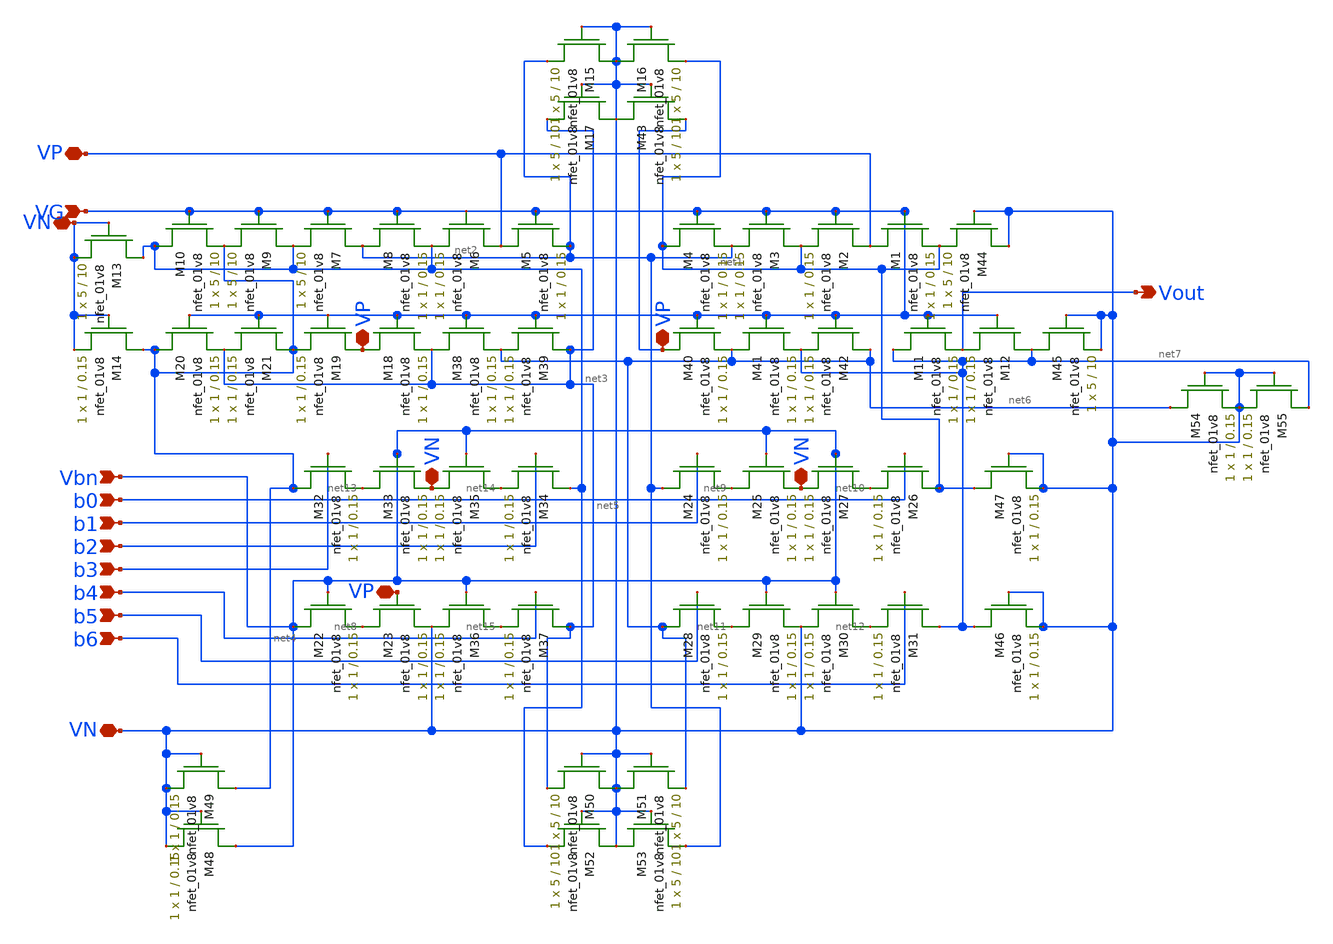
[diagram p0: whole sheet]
** sch_path: DAC_layout_1.sch
**.subckt DAC_layout_1 VP VG Vbn VN b1 b0 b2 b3 b4 b5 b6 Vout VP VP VP VN VN VN
*.iopin VP
*.ipin VG
*.ipin Vbn
*.iopin VN
*.ipin b1
*.ipin b0
*.ipin b2
*.ipin b3
*.ipin b4
*.ipin b5
*.ipin b6
*.opin Vout
*.iopin VP
*.iopin VP
*.iopin VP
*.iopin VN
*.iopin VN
*.iopin VN
XM2 VP VG net1 GND sky130_fd_pr__nfet_01v8 L=0.15 W=1 nf=1 ad='int((nf+1)/2) * W/nf * 0.29' as='int((nf+2)/2) * W/nf * 0.29'
+ pd='2*int((nf+1)/2) * (W/nf + 0.29)' ps='2*int((nf+2)/2) * (W/nf + 0.29)' nrd='0.29 / W' nrs='0.29 / W'
+ sa=0 sb=0 sd=0 mult=1 m=1
XM1 VP VG net1 GND sky130_fd_pr__nfet_01v8 L=0.15 W=1 nf=1 ad='int((nf+1)/2) * W/nf * 0.29' as='int((nf+2)/2) * W/nf * 0.29'
+ pd='2*int((nf+1)/2) * (W/nf + 0.29)' ps='2*int((nf+2)/2) * (W/nf + 0.29)' nrd='0.29 / W' nrs='0.29 / W'
+ sa=0 sb=0 sd=0 mult=1 m=1
XM5 VP VG net2 GND sky130_fd_pr__nfet_01v8 L=0.15 W=1 nf=1 ad='int((nf+1)/2) * W/nf * 0.29' as='int((nf+2)/2) * W/nf * 0.29'
+ pd='2*int((nf+1)/2) * (W/nf + 0.29)' ps='2*int((nf+2)/2) * (W/nf + 0.29)' nrd='0.29 / W' nrs='0.29 / W'
+ sa=0 sb=0 sd=0 mult=1 m=1
XM6 VP VG net3 GND sky130_fd_pr__nfet_01v8 L=0.15 W=1 nf=1 ad='int((nf+1)/2) * W/nf * 0.29' as='int((nf+2)/2) * W/nf * 0.29'
+ pd='2*int((nf+1)/2) * (W/nf + 0.29)' ps='2*int((nf+2)/2) * (W/nf + 0.29)' nrd='0.29 / W' nrs='0.29 / W'
+ sa=0 sb=0 sd=0 mult=1 m=1
XM7 net2 VG net3 GND sky130_fd_pr__nfet_01v8 L=10 W=5 nf=1 ad='int((nf+1)/2) * W/nf * 0.29' as='int((nf+2)/2) * W/nf * 0.29'
+ pd='2*int((nf+1)/2) * (W/nf + 0.29)' ps='2*int((nf+2)/2) * (W/nf + 0.29)' nrd='0.29 / W' nrs='0.29 / W'
+ sa=0 sb=0 sd=0 mult=1 m=1
XM8 net2 VG net3 GND sky130_fd_pr__nfet_01v8 L=0.15 W=1 nf=1 ad='int((nf+1)/2) * W/nf * 0.29' as='int((nf+2)/2) * W/nf * 0.29'
+ pd='2*int((nf+1)/2) * (W/nf + 0.29)' ps='2*int((nf+2)/2) * (W/nf + 0.29)' nrd='0.29 / W' nrs='0.29 / W'
+ sa=0 sb=0 sd=0 mult=1 m=1
XM9 net3 VG net4 VN sky130_fd_pr__nfet_01v8 L=10 W=5 nf=1 ad='int((nf+1)/2) * W/nf * 0.29' as='int((nf+2)/2) * W/nf * 0.29'
+ pd='2*int((nf+1)/2) * (W/nf + 0.29)' ps='2*int((nf+2)/2) * (W/nf + 0.29)' nrd='0.29 / W' nrs='0.29 / W'
+ sa=0 sb=0 sd=0 mult=1 m=1
XM10 net3 VG net4 VN sky130_fd_pr__nfet_01v8 L=10 W=5 nf=1 ad='int((nf+1)/2) * W/nf * 0.29' as='int((nf+2)/2) * W/nf * 0.29'
+ pd='2*int((nf+1)/2) * (W/nf + 0.29)' ps='2*int((nf+2)/2) * (W/nf + 0.29)' nrd='0.29 / W' nrs='0.29 / W'
+ sa=0 sb=0 sd=0 mult=1 m=1
XM3 net1 VG net2 GND sky130_fd_pr__nfet_01v8 L=0.15 W=1 nf=1 ad='int((nf+1)/2) * W/nf * 0.29' as='int((nf+2)/2) * W/nf * 0.29'
+ pd='2*int((nf+1)/2) * (W/nf + 0.29)' ps='2*int((nf+2)/2) * (W/nf + 0.29)' nrd='0.29 / W' nrs='0.29 / W'
+ sa=0 sb=0 sd=0 mult=1 m=1
XM4 net1 VG net2 GND sky130_fd_pr__nfet_01v8 L=0.15 W=1 nf=1 ad='int((nf+1)/2) * W/nf * 0.29' as='int((nf+2)/2) * W/nf * 0.29'
+ pd='2*int((nf+1)/2) * (W/nf + 0.29)' ps='2*int((nf+2)/2) * (W/nf + 0.29)' nrd='0.29 / W' nrs='0.29 / W'
+ sa=0 sb=0 sd=0 mult=1 m=1
XM22 Vbn Vbn net8 GND sky130_fd_pr__nfet_01v8 L=0.15 W=1 nf=1 ad='int((nf+1)/2) * W/nf * 0.29' as='int((nf+2)/2) * W/nf * 0.29'
+ pd='2*int((nf+1)/2) * (W/nf + 0.29)' ps='2*int((nf+2)/2) * (W/nf + 0.29)' nrd='0.29 / W' nrs='0.29 / W'
+ sa=0 sb=0 sd=0 mult=1 m=1
XM23 net8 VP VN GND sky130_fd_pr__nfet_01v8 L=0.15 W=1 nf=1 ad='int((nf+1)/2) * W/nf * 0.29' as='int((nf+2)/2) * W/nf * 0.29'
+ pd='2*int((nf+1)/2) * (W/nf + 0.29)' ps='2*int((nf+2)/2) * (W/nf + 0.29)' nrd='0.29 / W' nrs='0.29 / W'
+ sa=0 sb=0 sd=0 mult=1 m=1
XM24 net2 b1 net9 GND sky130_fd_pr__nfet_01v8 L=0.15 W=1 nf=1 ad='int((nf+1)/2) * W/nf * 0.29' as='int((nf+2)/2) * W/nf * 0.29'
+ pd='2*int((nf+1)/2) * (W/nf + 0.29)' ps='2*int((nf+2)/2) * (W/nf + 0.29)' nrd='0.29 / W' nrs='0.29 / W'
+ sa=0 sb=0 sd=0 mult=1 m=1
XM25 net9 Vbn VN GND sky130_fd_pr__nfet_01v8 L=0.15 W=1 nf=1 ad='int((nf+1)/2) * W/nf * 0.29' as='int((nf+2)/2) * W/nf * 0.29'
+ pd='2*int((nf+1)/2) * (W/nf + 0.29)' ps='2*int((nf+2)/2) * (W/nf + 0.29)' nrd='0.29 / W' nrs='0.29 / W'
+ sa=0 sb=0 sd=0 mult=1 m=1
XM26 net1 b0 net10 GND sky130_fd_pr__nfet_01v8 L=0.15 W=1 nf=1 ad='int((nf+1)/2) * W/nf * 0.29' as='int((nf+2)/2) * W/nf * 0.29'
+ pd='2*int((nf+1)/2) * (W/nf + 0.29)' ps='2*int((nf+2)/2) * (W/nf + 0.29)' nrd='0.29 / W' nrs='0.29 / W'
+ sa=0 sb=0 sd=0 mult=1 m=1
XM27 net10 Vbn VN GND sky130_fd_pr__nfet_01v8 L=0.15 W=1 nf=1 ad='int((nf+1)/2) * W/nf * 0.29' as='int((nf+2)/2) * W/nf * 0.29'
+ pd='2*int((nf+1)/2) * (W/nf + 0.29)' ps='2*int((nf+2)/2) * (W/nf + 0.29)' nrd='0.29 / W' nrs='0.29 / W'
+ sa=0 sb=0 sd=0 mult=1 m=1
XM28 net6 b5 net11 GND sky130_fd_pr__nfet_01v8 L=0.15 W=1 nf=1 ad='int((nf+1)/2) * W/nf * 0.29' as='int((nf+2)/2) * W/nf * 0.29'
+ pd='2*int((nf+1)/2) * (W/nf + 0.29)' ps='2*int((nf+2)/2) * (W/nf + 0.29)' nrd='0.29 / W' nrs='0.29 / W'
+ sa=0 sb=0 sd=0 mult=1 m=1
XM29 net11 Vbn VN GND sky130_fd_pr__nfet_01v8 L=0.15 W=1 nf=1 ad='int((nf+1)/2) * W/nf * 0.29' as='int((nf+2)/2) * W/nf * 0.29'
+ pd='2*int((nf+1)/2) * (W/nf + 0.29)' ps='2*int((nf+2)/2) * (W/nf + 0.29)' nrd='0.29 / W' nrs='0.29 / W'
+ sa=0 sb=0 sd=0 mult=1 m=1
XM30 net12 Vbn VN GND sky130_fd_pr__nfet_01v8 L=0.15 W=1 nf=1 ad='int((nf+1)/2) * W/nf * 0.29' as='int((nf+2)/2) * W/nf * 0.29'
+ pd='2*int((nf+1)/2) * (W/nf + 0.29)' ps='2*int((nf+2)/2) * (W/nf + 0.29)' nrd='0.29 / W' nrs='0.29 / W'
+ sa=0 sb=0 sd=0 mult=1 m=1
XM31 net7 b6 net12 GND sky130_fd_pr__nfet_01v8 L=0.15 W=1 nf=1 ad='int((nf+1)/2) * W/nf * 0.29' as='int((nf+2)/2) * W/nf * 0.29'
+ pd='2*int((nf+1)/2) * (W/nf + 0.29)' ps='2*int((nf+2)/2) * (W/nf + 0.29)' nrd='0.29 / W' nrs='0.29 / W'
+ sa=0 sb=0 sd=0 mult=1 m=1
XM32 net4 b3 net13 GND sky130_fd_pr__nfet_01v8 L=0.15 W=1 nf=1 ad='int((nf+1)/2) * W/nf * 0.29' as='int((nf+2)/2) * W/nf * 0.29'
+ pd='2*int((nf+1)/2) * (W/nf + 0.29)' ps='2*int((nf+2)/2) * (W/nf + 0.29)' nrd='0.29 / W' nrs='0.29 / W'
+ sa=0 sb=0 sd=0 mult=1 m=1
XM33 net13 Vbn VN GND sky130_fd_pr__nfet_01v8 L=0.15 W=1 nf=1 ad='int((nf+1)/2) * W/nf * 0.29' as='int((nf+2)/2) * W/nf * 0.29'
+ pd='2*int((nf+1)/2) * (W/nf + 0.29)' ps='2*int((nf+2)/2) * (W/nf + 0.29)' nrd='0.29 / W' nrs='0.29 / W'
+ sa=0 sb=0 sd=0 mult=1 m=1
XM34 net3 b2 net14 GND sky130_fd_pr__nfet_01v8 L=0.15 W=1 nf=1 ad='int((nf+1)/2) * W/nf * 0.29' as='int((nf+2)/2) * W/nf * 0.29'
+ pd='2*int((nf+1)/2) * (W/nf + 0.29)' ps='2*int((nf+2)/2) * (W/nf + 0.29)' nrd='0.29 / W' nrs='0.29 / W'
+ sa=0 sb=0 sd=0 mult=1 m=1
XM35 net14 Vbn VN GND sky130_fd_pr__nfet_01v8 L=0.15 W=1 nf=1 ad='int((nf+1)/2) * W/nf * 0.29' as='int((nf+2)/2) * W/nf * 0.29'
+ pd='2*int((nf+1)/2) * (W/nf + 0.29)' ps='2*int((nf+2)/2) * (W/nf + 0.29)' nrd='0.29 / W' nrs='0.29 / W'
+ sa=0 sb=0 sd=0 mult=1 m=1
XM36 net15 Vbn VN GND sky130_fd_pr__nfet_01v8 L=0.15 W=1 nf=1 ad='int((nf+1)/2) * W/nf * 0.29' as='int((nf+2)/2) * W/nf * 0.29'
+ pd='2*int((nf+1)/2) * (W/nf + 0.29)' ps='2*int((nf+2)/2) * (W/nf + 0.29)' nrd='0.29 / W' nrs='0.29 / W'
+ sa=0 sb=0 sd=0 mult=1 m=1
XM37 net5 b4 net15 GND sky130_fd_pr__nfet_01v8 L=0.15 W=1 nf=1 ad='int((nf+1)/2) * W/nf * 0.29' as='int((nf+2)/2) * W/nf * 0.29'
+ pd='2*int((nf+1)/2) * (W/nf + 0.29)' ps='2*int((nf+2)/2) * (W/nf + 0.29)' nrd='0.29 / W' nrs='0.29 / W'
+ sa=0 sb=0 sd=0 mult=1 m=1
XM18 VP VG net5 GND sky130_fd_pr__nfet_01v8 L=0.15 W=1 nf=1 ad='int((nf+1)/2) * W/nf * 0.29' as='int((nf+2)/2) * W/nf * 0.29'
+ pd='2*int((nf+1)/2) * (W/nf + 0.29)' ps='2*int((nf+2)/2) * (W/nf + 0.29)' nrd='0.29 / W' nrs='0.29 / W'
+ sa=0 sb=0 sd=0 mult=1 m=1
XM19 VP VG net4 GND sky130_fd_pr__nfet_01v8 L=0.15 W=1 nf=1 ad='int((nf+1)/2) * W/nf * 0.29' as='int((nf+2)/2) * W/nf * 0.29'
+ pd='2*int((nf+1)/2) * (W/nf + 0.29)' ps='2*int((nf+2)/2) * (W/nf + 0.29)' nrd='0.29 / W' nrs='0.29 / W'
+ sa=0 sb=0 sd=0 mult=1 m=1
XM20 net4 VG net5 GND sky130_fd_pr__nfet_01v8 L=0.15 W=1 nf=1 ad='int((nf+1)/2) * W/nf * 0.29' as='int((nf+2)/2) * W/nf * 0.29'
+ pd='2*int((nf+1)/2) * (W/nf + 0.29)' ps='2*int((nf+2)/2) * (W/nf + 0.29)' nrd='0.29 / W' nrs='0.29 / W'
+ sa=0 sb=0 sd=0 mult=1 m=1
XM21 net4 VG net5 GND sky130_fd_pr__nfet_01v8 L=0.15 W=1 nf=1 ad='int((nf+1)/2) * W/nf * 0.29' as='int((nf+2)/2) * W/nf * 0.29'
+ pd='2*int((nf+1)/2) * (W/nf + 0.29)' ps='2*int((nf+2)/2) * (W/nf + 0.29)' nrd='0.29 / W' nrs='0.29 / W'
+ sa=0 sb=0 sd=0 mult=1 m=1
XM38 net5 VG net6 GND sky130_fd_pr__nfet_01v8 L=0.15 W=1 nf=1 ad='int((nf+1)/2) * W/nf * 0.29' as='int((nf+2)/2) * W/nf * 0.29'
+ pd='2*int((nf+1)/2) * (W/nf + 0.29)' ps='2*int((nf+2)/2) * (W/nf + 0.29)' nrd='0.29 / W' nrs='0.29 / W'
+ sa=0 sb=0 sd=0 mult=1 m=1
XM39 net5 VG net6 GND sky130_fd_pr__nfet_01v8 L=0.15 W=1 nf=1 ad='int((nf+1)/2) * W/nf * 0.29' as='int((nf+2)/2) * W/nf * 0.29'
+ pd='2*int((nf+1)/2) * (W/nf + 0.29)' ps='2*int((nf+2)/2) * (W/nf + 0.29)' nrd='0.29 / W' nrs='0.29 / W'
+ sa=0 sb=0 sd=0 mult=1 m=1
XM40 VP VG net6 GND sky130_fd_pr__nfet_01v8 L=0.15 W=1 nf=1 ad='int((nf+1)/2) * W/nf * 0.29' as='int((nf+2)/2) * W/nf * 0.29'
+ pd='2*int((nf+1)/2) * (W/nf + 0.29)' ps='2*int((nf+2)/2) * (W/nf + 0.29)' nrd='0.29 / W' nrs='0.29 / W'
+ sa=0 sb=0 sd=0 mult=1 m=1
XM41 net6 VG net7 GND sky130_fd_pr__nfet_01v8 L=0.15 W=1 nf=1 ad='int((nf+1)/2) * W/nf * 0.29' as='int((nf+2)/2) * W/nf * 0.29'
+ pd='2*int((nf+1)/2) * (W/nf + 0.29)' ps='2*int((nf+2)/2) * (W/nf + 0.29)' nrd='0.29 / W' nrs='0.29 / W'
+ sa=0 sb=0 sd=0 mult=1 m=1
XM42 net6 VG net7 GND sky130_fd_pr__nfet_01v8 L=0.15 W=1 nf=1 ad='int((nf+1)/2) * W/nf * 0.29' as='int((nf+2)/2) * W/nf * 0.29'
+ pd='2*int((nf+1)/2) * (W/nf + 0.29)' ps='2*int((nf+2)/2) * (W/nf + 0.29)' nrd='0.29 / W' nrs='0.29 / W'
+ sa=0 sb=0 sd=0 mult=1 m=1
XM11 net7 VG Vout GND sky130_fd_pr__nfet_01v8 L=0.15 W=1 nf=1 ad='int((nf+1)/2) * W/nf * 0.29' as='int((nf+2)/2) * W/nf * 0.29'
+ pd='2*int((nf+1)/2) * (W/nf + 0.29)' ps='2*int((nf+2)/2) * (W/nf + 0.29)' nrd='0.29 / W' nrs='0.29 / W'
+ sa=0 sb=0 sd=0 mult=1 m=1
XM12 net7 VG Vout GND sky130_fd_pr__nfet_01v8 L=0.15 W=1 nf=1 ad='int((nf+1)/2) * W/nf * 0.29' as='int((nf+2)/2) * W/nf * 0.29'
+ pd='2*int((nf+1)/2) * (W/nf + 0.29)' ps='2*int((nf+2)/2) * (W/nf + 0.29)' nrd='0.29 / W' nrs='0.29 / W'
+ sa=0 sb=0 sd=0 mult=1 m=1
XM13 net3 VN VN VN sky130_fd_pr__nfet_01v8 L=10 W=5 nf=1 ad='int((nf+1)/2) * W/nf * 0.29' as='int((nf+2)/2) * W/nf * 0.29'
+ pd='2*int((nf+1)/2) * (W/nf + 0.29)' ps='2*int((nf+2)/2) * (W/nf + 0.29)' nrd='0.29 / W' nrs='0.29 / W'
+ sa=0 sb=0 sd=0 mult=1 m=1
XM14 net4 VN VN GND sky130_fd_pr__nfet_01v8 L=0.15 W=1 nf=1 ad='int((nf+1)/2) * W/nf * 0.29' as='int((nf+2)/2) * W/nf * 0.29'
+ pd='2*int((nf+1)/2) * (W/nf + 0.29)' ps='2*int((nf+2)/2) * (W/nf + 0.29)' nrd='0.29 / W' nrs='0.29 / W'
+ sa=0 sb=0 sd=0 mult=1 m=1
XM15 VN VN net2 GND sky130_fd_pr__nfet_01v8 L=10 W=5 nf=1 ad='int((nf+1)/2) * W/nf * 0.29' as='int((nf+2)/2) * W/nf * 0.29'
+ pd='2*int((nf+1)/2) * (W/nf + 0.29)' ps='2*int((nf+2)/2) * (W/nf + 0.29)' nrd='0.29 / W' nrs='0.29 / W'
+ sa=0 sb=0 sd=0 mult=1 m=1
XM16 VN VN net1 GND sky130_fd_pr__nfet_01v8 L=10 W=5 nf=1 ad='int((nf+1)/2) * W/nf * 0.29' as='int((nf+2)/2) * W/nf * 0.29'
+ pd='2*int((nf+1)/2) * (W/nf + 0.29)' ps='2*int((nf+2)/2) * (W/nf + 0.29)' nrd='0.29 / W' nrs='0.29 / W'
+ sa=0 sb=0 sd=0 mult=1 m=1
XM17 VN VN net5 GND sky130_fd_pr__nfet_01v8 L=10 W=5 nf=1 ad='int((nf+1)/2) * W/nf * 0.29' as='int((nf+2)/2) * W/nf * 0.29'
+ pd='2*int((nf+1)/2) * (W/nf + 0.29)' ps='2*int((nf+2)/2) * (W/nf + 0.29)' nrd='0.29 / W' nrs='0.29 / W'
+ sa=0 sb=0 sd=0 mult=1 m=1
XM43 VN VN VP GND sky130_fd_pr__nfet_01v8 L=10 W=5 nf=1 ad='int((nf+1)/2) * W/nf * 0.29' as='int((nf+2)/2) * W/nf * 0.29'
+ pd='2*int((nf+1)/2) * (W/nf + 0.29)' ps='2*int((nf+2)/2) * (W/nf + 0.29)' nrd='0.29 / W' nrs='0.29 / W'
+ sa=0 sb=0 sd=0 mult=1 m=1
XM44 VN VN net1 GND sky130_fd_pr__nfet_01v8 L=10 W=5 nf=1 ad='int((nf+1)/2) * W/nf * 0.29' as='int((nf+2)/2) * W/nf * 0.29'
+ pd='2*int((nf+1)/2) * (W/nf + 0.29)' ps='2*int((nf+2)/2) * (W/nf + 0.29)' nrd='0.29 / W' nrs='0.29 / W'
+ sa=0 sb=0 sd=0 mult=1 m=1
XM45 net7 VN VN GND sky130_fd_pr__nfet_01v8 L=10 W=5 nf=1 ad='int((nf+1)/2) * W/nf * 0.29' as='int((nf+2)/2) * W/nf * 0.29'
+ pd='2*int((nf+1)/2) * (W/nf + 0.29)' ps='2*int((nf+2)/2) * (W/nf + 0.29)' nrd='0.29 / W' nrs='0.29 / W'
+ sa=0 sb=0 sd=0 mult=1 m=1
XM46 net7 VN VN GND sky130_fd_pr__nfet_01v8 L=0.15 W=1 nf=1 ad='int((nf+1)/2) * W/nf * 0.29' as='int((nf+2)/2) * W/nf * 0.29'
+ pd='2*int((nf+1)/2) * (W/nf + 0.29)' ps='2*int((nf+2)/2) * (W/nf + 0.29)' nrd='0.29 / W' nrs='0.29 / W'
+ sa=0 sb=0 sd=0 mult=1 m=1
XM47 net1 VN VN GND sky130_fd_pr__nfet_01v8 L=0.15 W=1 nf=1 ad='int((nf+1)/2) * W/nf * 0.29' as='int((nf+2)/2) * W/nf * 0.29'
+ pd='2*int((nf+1)/2) * (W/nf + 0.29)' ps='2*int((nf+2)/2) * (W/nf + 0.29)' nrd='0.29 / W' nrs='0.29 / W'
+ sa=0 sb=0 sd=0 mult=1 m=1
XM48 Vbn VN VN GND sky130_fd_pr__nfet_01v8 L=0.15 W=1 nf=1 ad='int((nf+1)/2) * W/nf * 0.29' as='int((nf+2)/2) * W/nf * 0.29'
+ pd='2*int((nf+1)/2) * (W/nf + 0.29)' ps='2*int((nf+2)/2) * (W/nf + 0.29)' nrd='0.29 / W' nrs='0.29 / W'
+ sa=0 sb=0 sd=0 mult=1 m=1
XM49 net4 VN VN GND sky130_fd_pr__nfet_01v8 L=0.15 W=1 nf=1 ad='int((nf+1)/2) * W/nf * 0.29' as='int((nf+2)/2) * W/nf * 0.29'
+ pd='2*int((nf+1)/2) * (W/nf + 0.29)' ps='2*int((nf+2)/2) * (W/nf + 0.29)' nrd='0.29 / W' nrs='0.29 / W'
+ sa=0 sb=0 sd=0 mult=1 m=1
XM50 VN VN net5 GND sky130_fd_pr__nfet_01v8 L=10 W=5 nf=1 ad='int((nf+1)/2) * W/nf * 0.29' as='int((nf+2)/2) * W/nf * 0.29'
+ pd='2*int((nf+1)/2) * (W/nf + 0.29)' ps='2*int((nf+2)/2) * (W/nf + 0.29)' nrd='0.29 / W' nrs='0.29 / W'
+ sa=0 sb=0 sd=0 mult=1 m=1
XM51 VN VN net6 GND sky130_fd_pr__nfet_01v8 L=10 W=5 nf=1 ad='int((nf+1)/2) * W/nf * 0.29' as='int((nf+2)/2) * W/nf * 0.29'
+ pd='2*int((nf+1)/2) * (W/nf + 0.29)' ps='2*int((nf+2)/2) * (W/nf + 0.29)' nrd='0.29 / W' nrs='0.29 / W'
+ sa=0 sb=0 sd=0 mult=1 m=1
XM52 VN VN net3 GND sky130_fd_pr__nfet_01v8 L=10 W=5 nf=1 ad='int((nf+1)/2) * W/nf * 0.29' as='int((nf+2)/2) * W/nf * 0.29'
+ pd='2*int((nf+1)/2) * (W/nf + 0.29)' ps='2*int((nf+2)/2) * (W/nf + 0.29)' nrd='0.29 / W' nrs='0.29 / W'
+ sa=0 sb=0 sd=0 mult=1 m=1
XM53 VN VN net2 GND sky130_fd_pr__nfet_01v8 L=10 W=5 nf=1 ad='int((nf+1)/2) * W/nf * 0.29' as='int((nf+2)/2) * W/nf * 0.29'
+ pd='2*int((nf+1)/2) * (W/nf + 0.29)' ps='2*int((nf+2)/2) * (W/nf + 0.29)' nrd='0.29 / W' nrs='0.29 / W'
+ sa=0 sb=0 sd=0 mult=1 m=1
XM54 net6 VN VN GND sky130_fd_pr__nfet_01v8 L=0.15 W=1 nf=1 ad='int((nf+1)/2) * W/nf * 0.29' as='int((nf+2)/2) * W/nf * 0.29'
+ pd='2*int((nf+1)/2) * (W/nf + 0.29)' ps='2*int((nf+2)/2) * (W/nf + 0.29)' nrd='0.29 / W' nrs='0.29 / W'
+ sa=0 sb=0 sd=0 mult=1 m=1
XM55 net7 VN VN GND sky130_fd_pr__nfet_01v8 L=0.15 W=1 nf=1 ad='int((nf+1)/2) * W/nf * 0.29' as='int((nf+2)/2) * W/nf * 0.29'
+ pd='2*int((nf+1)/2) * (W/nf + 0.29)' ps='2*int((nf+2)/2) * (W/nf + 0.29)' nrd='0.29 / W' nrs='0.29 / W'
+ sa=0 sb=0 sd=0 mult=1 m=1
**.ends
.end
